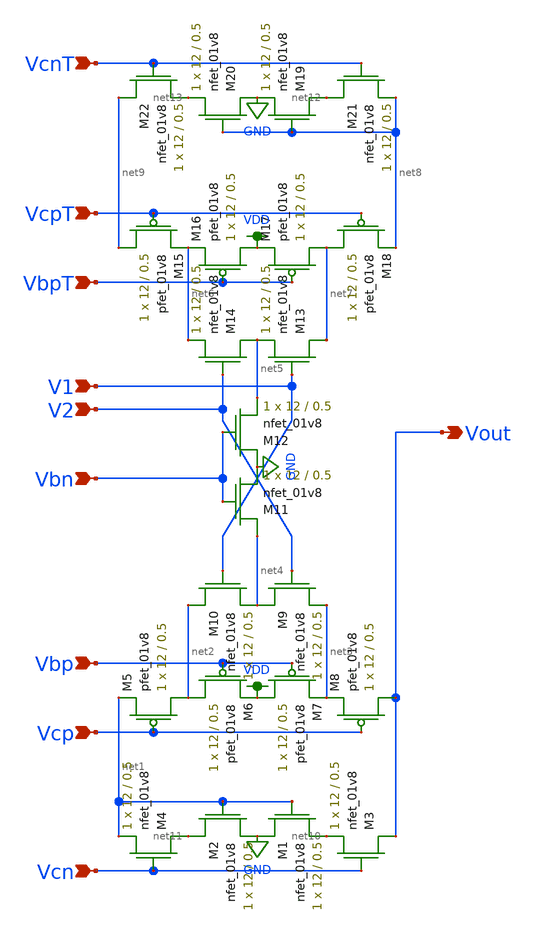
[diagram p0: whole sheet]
** sch_path: mp3/schematics/fcda_lds.sch
**.subckt fcda_lds Vcn Vcp Vbp Vbn V2 V1 VbpT VcpT VcnT Vout
*.ipin Vcn
*.ipin Vcp
*.ipin Vbp
*.ipin Vbn
*.ipin V2
*.ipin V1
*.ipin VbpT
*.ipin VcpT
*.ipin VcnT
*.opin Vout
XM1 GND net1 net10 GND sky130_fd_pr__nfet_01v8 L=0.5 W=12 nf=1 ad='int((nf+1)/2) * W/nf * 0.29' as='int((nf+2)/2) * W/nf * 0.29'
+ pd='2*int((nf+1)/2) * (W/nf + 0.29)' ps='2*int((nf+2)/2) * (W/nf + 0.29)' nrd='0.29 / W' nrs='0.29 / W'
+ sa=0 sb=0 sd=0 mult=1 m=1
XM2 net11 net1 GND GND sky130_fd_pr__nfet_01v8 L=0.5 W=12 nf=1 ad='int((nf+1)/2) * W/nf * 0.29' as='int((nf+2)/2) * W/nf * 0.29'
+ pd='2*int((nf+1)/2) * (W/nf + 0.29)' ps='2*int((nf+2)/2) * (W/nf + 0.29)' nrd='0.29 / W' nrs='0.29 / W'
+ sa=0 sb=0 sd=0 mult=1 m=1
XM3 Vout Vcn net10 GND sky130_fd_pr__nfet_01v8 L=0.5 W=12 nf=1 ad='int((nf+1)/2) * W/nf * 0.29' as='int((nf+2)/2) * W/nf * 0.29'
+ pd='2*int((nf+1)/2) * (W/nf + 0.29)' ps='2*int((nf+2)/2) * (W/nf + 0.29)' nrd='0.29 / W' nrs='0.29 / W'
+ sa=0 sb=0 sd=0 mult=1 m=1
XM4 net11 Vcn net1 GND sky130_fd_pr__nfet_01v8 L=0.5 W=12 nf=1 ad='int((nf+1)/2) * W/nf * 0.29' as='int((nf+2)/2) * W/nf * 0.29'
+ pd='2*int((nf+1)/2) * (W/nf + 0.29)' ps='2*int((nf+2)/2) * (W/nf + 0.29)' nrd='0.29 / W' nrs='0.29 / W'
+ sa=0 sb=0 sd=0 mult=1 m=1
XM5 net2 Vcp net1 VDD sky130_fd_pr__pfet_01v8 L=0.5 W=12 nf=1 ad='int((nf+1)/2) * W/nf * 0.29' as='int((nf+2)/2) * W/nf * 0.29'
+ pd='2*int((nf+1)/2) * (W/nf + 0.29)' ps='2*int((nf+2)/2) * (W/nf + 0.29)' nrd='0.29 / W' nrs='0.29 / W'
+ sa=0 sb=0 sd=0 mult=1 m=1
XM6 net2 Vbp VDD VDD sky130_fd_pr__pfet_01v8 L=0.5 W=12 nf=1 ad='int((nf+1)/2) * W/nf * 0.29' as='int((nf+2)/2) * W/nf * 0.29'
+ pd='2*int((nf+1)/2) * (W/nf + 0.29)' ps='2*int((nf+2)/2) * (W/nf + 0.29)' nrd='0.29 / W' nrs='0.29 / W'
+ sa=0 sb=0 sd=0 mult=1 m=1
XM7 VDD Vbp net3 VDD sky130_fd_pr__pfet_01v8 L=0.5 W=12 nf=1 ad='int((nf+1)/2) * W/nf * 0.29' as='int((nf+2)/2) * W/nf * 0.29'
+ pd='2*int((nf+1)/2) * (W/nf + 0.29)' ps='2*int((nf+2)/2) * (W/nf + 0.29)' nrd='0.29 / W' nrs='0.29 / W'
+ sa=0 sb=0 sd=0 mult=1 m=1
XM8 Vout Vcp net3 VDD sky130_fd_pr__pfet_01v8 L=0.5 W=12 nf=1 ad='int((nf+1)/2) * W/nf * 0.29' as='int((nf+2)/2) * W/nf * 0.29'
+ pd='2*int((nf+1)/2) * (W/nf + 0.29)' ps='2*int((nf+2)/2) * (W/nf + 0.29)' nrd='0.29 / W' nrs='0.29 / W'
+ sa=0 sb=0 sd=0 mult=1 m=1
XM9 net4 V2 net3 GND sky130_fd_pr__nfet_01v8 L=0.5 W=12 nf=1 ad='int((nf+1)/2) * W/nf * 0.29' as='int((nf+2)/2) * W/nf * 0.29'
+ pd='2*int((nf+1)/2) * (W/nf + 0.29)' ps='2*int((nf+2)/2) * (W/nf + 0.29)' nrd='0.29 / W' nrs='0.29 / W'
+ sa=0 sb=0 sd=0 mult=1 m=1
XM10 net2 V1 net4 GND sky130_fd_pr__nfet_01v8 L=0.5 W=12 nf=1 ad='int((nf+1)/2) * W/nf * 0.29' as='int((nf+2)/2) * W/nf * 0.29'
+ pd='2*int((nf+1)/2) * (W/nf + 0.29)' ps='2*int((nf+2)/2) * (W/nf + 0.29)' nrd='0.29 / W' nrs='0.29 / W'
+ sa=0 sb=0 sd=0 mult=1 m=1
XM11 net4 Vbn GND GND sky130_fd_pr__nfet_01v8 L=0.5 W=12 nf=1 ad='int((nf+1)/2) * W/nf * 0.29' as='int((nf+2)/2) * W/nf * 0.29'
+ pd='2*int((nf+1)/2) * (W/nf + 0.29)' ps='2*int((nf+2)/2) * (W/nf + 0.29)' nrd='0.29 / W' nrs='0.29 / W'
+ sa=0 sb=0 sd=0 mult=1 m=1
XM12 GND Vbn net5 GND sky130_fd_pr__nfet_01v8 L=0.5 W=12 nf=1 ad='int((nf+1)/2) * W/nf * 0.29' as='int((nf+2)/2) * W/nf * 0.29'
+ pd='2*int((nf+1)/2) * (W/nf + 0.29)' ps='2*int((nf+2)/2) * (W/nf + 0.29)' nrd='0.29 / W' nrs='0.29 / W'
+ sa=0 sb=0 sd=0 mult=1 m=1
XM13 net7 V1 net5 GND sky130_fd_pr__nfet_01v8 L=0.5 W=12 nf=1 ad='int((nf+1)/2) * W/nf * 0.29' as='int((nf+2)/2) * W/nf * 0.29'
+ pd='2*int((nf+1)/2) * (W/nf + 0.29)' ps='2*int((nf+2)/2) * (W/nf + 0.29)' nrd='0.29 / W' nrs='0.29 / W'
+ sa=0 sb=0 sd=0 mult=1 m=1
XM14 net5 V2 net6 GND sky130_fd_pr__nfet_01v8 L=0.5 W=12 nf=1 ad='int((nf+1)/2) * W/nf * 0.29' as='int((nf+2)/2) * W/nf * 0.29'
+ pd='2*int((nf+1)/2) * (W/nf + 0.29)' ps='2*int((nf+2)/2) * (W/nf + 0.29)' nrd='0.29 / W' nrs='0.29 / W'
+ sa=0 sb=0 sd=0 mult=1 m=1
XM15 net9 VcpT net6 VDD sky130_fd_pr__pfet_01v8 L=0.5 W=12 nf=1 ad='int((nf+1)/2) * W/nf * 0.29' as='int((nf+2)/2) * W/nf * 0.29'
+ pd='2*int((nf+1)/2) * (W/nf + 0.29)' ps='2*int((nf+2)/2) * (W/nf + 0.29)' nrd='0.29 / W' nrs='0.29 / W'
+ sa=0 sb=0 sd=0 mult=1 m=1
XM16 VDD VbpT net6 VDD sky130_fd_pr__pfet_01v8 L=0.5 W=12 nf=1 ad='int((nf+1)/2) * W/nf * 0.29' as='int((nf+2)/2) * W/nf * 0.29'
+ pd='2*int((nf+1)/2) * (W/nf + 0.29)' ps='2*int((nf+2)/2) * (W/nf + 0.29)' nrd='0.29 / W' nrs='0.29 / W'
+ sa=0 sb=0 sd=0 mult=1 m=1
XM17 net7 VbpT VDD VDD sky130_fd_pr__pfet_01v8 L=0.5 W=12 nf=1 ad='int((nf+1)/2) * W/nf * 0.29' as='int((nf+2)/2) * W/nf * 0.29'
+ pd='2*int((nf+1)/2) * (W/nf + 0.29)' ps='2*int((nf+2)/2) * (W/nf + 0.29)' nrd='0.29 / W' nrs='0.29 / W'
+ sa=0 sb=0 sd=0 mult=1 m=1
XM18 net7 VcpT net8 VDD sky130_fd_pr__pfet_01v8 L=0.5 W=12 nf=1 ad='int((nf+1)/2) * W/nf * 0.29' as='int((nf+2)/2) * W/nf * 0.29'
+ pd='2*int((nf+1)/2) * (W/nf + 0.29)' ps='2*int((nf+2)/2) * (W/nf + 0.29)' nrd='0.29 / W' nrs='0.29 / W'
+ sa=0 sb=0 sd=0 mult=1 m=1
XM19 net12 net8 GND GND sky130_fd_pr__nfet_01v8 L=0.5 W=12 nf=1 ad='int((nf+1)/2) * W/nf * 0.29' as='int((nf+2)/2) * W/nf * 0.29'
+ pd='2*int((nf+1)/2) * (W/nf + 0.29)' ps='2*int((nf+2)/2) * (W/nf + 0.29)' nrd='0.29 / W' nrs='0.29 / W'
+ sa=0 sb=0 sd=0 mult=1 m=1
XM20 GND net8 net13 GND sky130_fd_pr__nfet_01v8 L=0.5 W=12 nf=1 ad='int((nf+1)/2) * W/nf * 0.29' as='int((nf+2)/2) * W/nf * 0.29'
+ pd='2*int((nf+1)/2) * (W/nf + 0.29)' ps='2*int((nf+2)/2) * (W/nf + 0.29)' nrd='0.29 / W' nrs='0.29 / W'
+ sa=0 sb=0 sd=0 mult=1 m=1
XM21 net12 VcnT net8 GND sky130_fd_pr__nfet_01v8 L=0.5 W=12 nf=1 ad='int((nf+1)/2) * W/nf * 0.29' as='int((nf+2)/2) * W/nf * 0.29'
+ pd='2*int((nf+1)/2) * (W/nf + 0.29)' ps='2*int((nf+2)/2) * (W/nf + 0.29)' nrd='0.29 / W' nrs='0.29 / W'
+ sa=0 sb=0 sd=0 mult=1 m=1
XM22 net9 VcnT net13 GND sky130_fd_pr__nfet_01v8 L=0.5 W=12 nf=1 ad='int((nf+1)/2) * W/nf * 0.29' as='int((nf+2)/2) * W/nf * 0.29'
+ pd='2*int((nf+1)/2) * (W/nf + 0.29)' ps='2*int((nf+2)/2) * (W/nf + 0.29)' nrd='0.29 / W' nrs='0.29 / W'
+ sa=0 sb=0 sd=0 mult=1 m=1
**.ends
.GLOBAL GND
.GLOBAL VDD
.end
